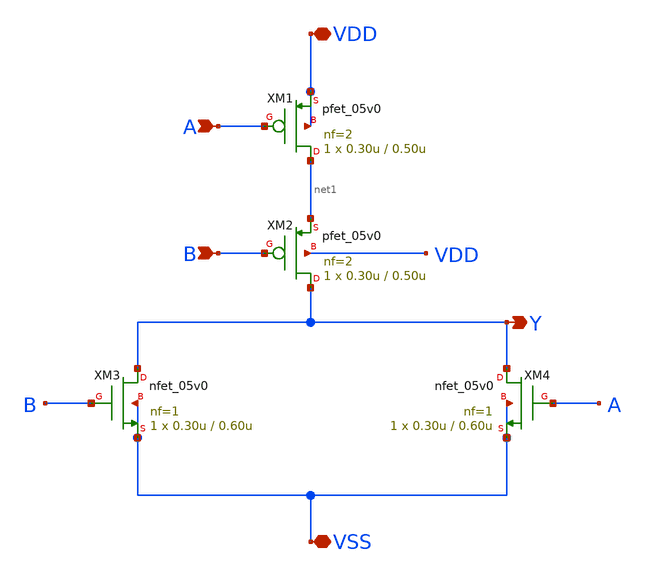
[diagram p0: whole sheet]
** sch_path: designs/libs/core_test/test_nor/test_nor.sch
**.subckt test_nor VDD VSS Y A B
*.iopin VDD
*.iopin VSS
*.opin Y
*.ipin A
*.ipin B
XM1 net1 A VDD VDD pfet_05v0 L=0.50u W=0.30u nf=2 ad='int((nf+1)/2) * W/nf * 0.18u' as='int((nf+2)/2) * W/nf * 0.18u'
+ pd='2*int((nf+1)/2) * (W/nf + 0.18u)' ps='2*int((nf+2)/2) * (W/nf + 0.18u)' nrd='0.18u / W' nrs='0.18u / W'
+ sa=0 sb=0 sd=0 m=1
XM3 Y B VSS VSS nfet_05v0 L=0.60u W=0.30u nf=1 ad='int((nf+1)/2) * W/nf * 0.18u' as='int((nf+2)/2) * W/nf * 0.18u'
+ pd='2*int((nf+1)/2) * (W/nf + 0.18u)' ps='2*int((nf+2)/2) * (W/nf + 0.18u)' nrd='0.18u / W' nrs='0.18u / W'
+ sa=0 sb=0 sd=0 m=1
XM2 Y B net1 VDD pfet_05v0 L=0.50u W=0.30u nf=2 ad='int((nf+1)/2) * W/nf * 0.18u' as='int((nf+2)/2) * W/nf * 0.18u'
+ pd='2*int((nf+1)/2) * (W/nf + 0.18u)' ps='2*int((nf+2)/2) * (W/nf + 0.18u)' nrd='0.18u / W' nrs='0.18u / W'
+ sa=0 sb=0 sd=0 m=1
XM4 Y A VSS VSS nfet_05v0 L=0.60u W=0.30u nf=1 ad='int((nf+1)/2) * W/nf * 0.18u' as='int((nf+2)/2) * W/nf * 0.18u'
+ pd='2*int((nf+1)/2) * (W/nf + 0.18u)' ps='2*int((nf+2)/2) * (W/nf + 0.18u)' nrd='0.18u / W' nrs='0.18u / W'
+ sa=0 sb=0 sd=0 m=1
**.ends
.end
